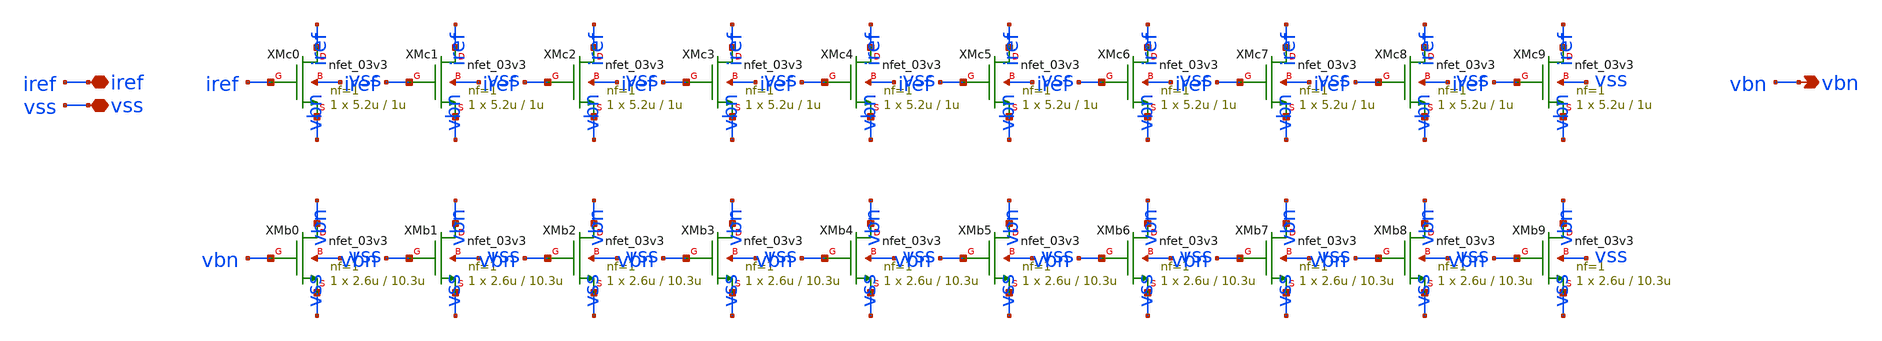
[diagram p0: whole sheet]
** sch_path: design/analog/bias.sch
**.subckt bias iref vss vbn
*.iopin iref
*.iopin vss
*.opin vbn
XMc0 iref iref vbn vss nfet_03v3 L=1u W=5.2u nf=1 ad='int((nf+1)/2) * W/nf * 0.18u' as='int((nf+2)/2) * W/nf * 0.18u'
+ pd='2*int((nf+1)/2) * (W/nf + 0.18u)' ps='2*int((nf+2)/2) * (W/nf + 0.18u)' nrd='0.18u / W' nrs='0.18u / W'
+ sa=0 sb=0 sd=0 m=1
XMb0 vbn vbn vss vss nfet_03v3 L=10.3u W=2.6u nf=1 ad='int((nf+1)/2) * W/nf * 0.18u' as='int((nf+2)/2) * W/nf * 0.18u'
+ pd='2*int((nf+1)/2) * (W/nf + 0.18u)' ps='2*int((nf+2)/2) * (W/nf + 0.18u)' nrd='0.18u / W' nrs='0.18u / W'
+ sa=0 sb=0 sd=0 m=1
XMc1 iref iref vbn vss nfet_03v3 L=1u W=5.2u nf=1 ad='int((nf+1)/2) * W/nf * 0.18u' as='int((nf+2)/2) * W/nf * 0.18u'
+ pd='2*int((nf+1)/2) * (W/nf + 0.18u)' ps='2*int((nf+2)/2) * (W/nf + 0.18u)' nrd='0.18u / W' nrs='0.18u / W'
+ sa=0 sb=0 sd=0 m=1
XMb1 vbn vbn vss vss nfet_03v3 L=10.3u W=2.6u nf=1 ad='int((nf+1)/2) * W/nf * 0.18u' as='int((nf+2)/2) * W/nf * 0.18u'
+ pd='2*int((nf+1)/2) * (W/nf + 0.18u)' ps='2*int((nf+2)/2) * (W/nf + 0.18u)' nrd='0.18u / W' nrs='0.18u / W'
+ sa=0 sb=0 sd=0 m=1
XMc2 iref iref vbn vss nfet_03v3 L=1u W=5.2u nf=1 ad='int((nf+1)/2) * W/nf * 0.18u' as='int((nf+2)/2) * W/nf * 0.18u'
+ pd='2*int((nf+1)/2) * (W/nf + 0.18u)' ps='2*int((nf+2)/2) * (W/nf + 0.18u)' nrd='0.18u / W' nrs='0.18u / W'
+ sa=0 sb=0 sd=0 m=1
XMb2 vbn vbn vss vss nfet_03v3 L=10.3u W=2.6u nf=1 ad='int((nf+1)/2) * W/nf * 0.18u' as='int((nf+2)/2) * W/nf * 0.18u'
+ pd='2*int((nf+1)/2) * (W/nf + 0.18u)' ps='2*int((nf+2)/2) * (W/nf + 0.18u)' nrd='0.18u / W' nrs='0.18u / W'
+ sa=0 sb=0 sd=0 m=1
XMc3 iref iref vbn vss nfet_03v3 L=1u W=5.2u nf=1 ad='int((nf+1)/2) * W/nf * 0.18u' as='int((nf+2)/2) * W/nf * 0.18u'
+ pd='2*int((nf+1)/2) * (W/nf + 0.18u)' ps='2*int((nf+2)/2) * (W/nf + 0.18u)' nrd='0.18u / W' nrs='0.18u / W'
+ sa=0 sb=0 sd=0 m=1
XMb3 vbn vbn vss vss nfet_03v3 L=10.3u W=2.6u nf=1 ad='int((nf+1)/2) * W/nf * 0.18u' as='int((nf+2)/2) * W/nf * 0.18u'
+ pd='2*int((nf+1)/2) * (W/nf + 0.18u)' ps='2*int((nf+2)/2) * (W/nf + 0.18u)' nrd='0.18u / W' nrs='0.18u / W'
+ sa=0 sb=0 sd=0 m=1
XMc4 iref iref vbn vss nfet_03v3 L=1u W=5.2u nf=1 ad='int((nf+1)/2) * W/nf * 0.18u' as='int((nf+2)/2) * W/nf * 0.18u'
+ pd='2*int((nf+1)/2) * (W/nf + 0.18u)' ps='2*int((nf+2)/2) * (W/nf + 0.18u)' nrd='0.18u / W' nrs='0.18u / W'
+ sa=0 sb=0 sd=0 m=1
XMb4 vbn vbn vss vss nfet_03v3 L=10.3u W=2.6u nf=1 ad='int((nf+1)/2) * W/nf * 0.18u' as='int((nf+2)/2) * W/nf * 0.18u'
+ pd='2*int((nf+1)/2) * (W/nf + 0.18u)' ps='2*int((nf+2)/2) * (W/nf + 0.18u)' nrd='0.18u / W' nrs='0.18u / W'
+ sa=0 sb=0 sd=0 m=1
XMc5 iref iref vbn vss nfet_03v3 L=1u W=5.2u nf=1 ad='int((nf+1)/2) * W/nf * 0.18u' as='int((nf+2)/2) * W/nf * 0.18u'
+ pd='2*int((nf+1)/2) * (W/nf + 0.18u)' ps='2*int((nf+2)/2) * (W/nf + 0.18u)' nrd='0.18u / W' nrs='0.18u / W'
+ sa=0 sb=0 sd=0 m=1
XMb5 vbn vbn vss vss nfet_03v3 L=10.3u W=2.6u nf=1 ad='int((nf+1)/2) * W/nf * 0.18u' as='int((nf+2)/2) * W/nf * 0.18u'
+ pd='2*int((nf+1)/2) * (W/nf + 0.18u)' ps='2*int((nf+2)/2) * (W/nf + 0.18u)' nrd='0.18u / W' nrs='0.18u / W'
+ sa=0 sb=0 sd=0 m=1
XMc6 iref iref vbn vss nfet_03v3 L=1u W=5.2u nf=1 ad='int((nf+1)/2) * W/nf * 0.18u' as='int((nf+2)/2) * W/nf * 0.18u'
+ pd='2*int((nf+1)/2) * (W/nf + 0.18u)' ps='2*int((nf+2)/2) * (W/nf + 0.18u)' nrd='0.18u / W' nrs='0.18u / W'
+ sa=0 sb=0 sd=0 m=1
XMb6 vbn vbn vss vss nfet_03v3 L=10.3u W=2.6u nf=1 ad='int((nf+1)/2) * W/nf * 0.18u' as='int((nf+2)/2) * W/nf * 0.18u'
+ pd='2*int((nf+1)/2) * (W/nf + 0.18u)' ps='2*int((nf+2)/2) * (W/nf + 0.18u)' nrd='0.18u / W' nrs='0.18u / W'
+ sa=0 sb=0 sd=0 m=1
XMc7 iref iref vbn vss nfet_03v3 L=1u W=5.2u nf=1 ad='int((nf+1)/2) * W/nf * 0.18u' as='int((nf+2)/2) * W/nf * 0.18u'
+ pd='2*int((nf+1)/2) * (W/nf + 0.18u)' ps='2*int((nf+2)/2) * (W/nf + 0.18u)' nrd='0.18u / W' nrs='0.18u / W'
+ sa=0 sb=0 sd=0 m=1
XMb7 vbn vbn vss vss nfet_03v3 L=10.3u W=2.6u nf=1 ad='int((nf+1)/2) * W/nf * 0.18u' as='int((nf+2)/2) * W/nf * 0.18u'
+ pd='2*int((nf+1)/2) * (W/nf + 0.18u)' ps='2*int((nf+2)/2) * (W/nf + 0.18u)' nrd='0.18u / W' nrs='0.18u / W'
+ sa=0 sb=0 sd=0 m=1
XMc8 iref iref vbn vss nfet_03v3 L=1u W=5.2u nf=1 ad='int((nf+1)/2) * W/nf * 0.18u' as='int((nf+2)/2) * W/nf * 0.18u'
+ pd='2*int((nf+1)/2) * (W/nf + 0.18u)' ps='2*int((nf+2)/2) * (W/nf + 0.18u)' nrd='0.18u / W' nrs='0.18u / W'
+ sa=0 sb=0 sd=0 m=1
XMb8 vbn vbn vss vss nfet_03v3 L=10.3u W=2.6u nf=1 ad='int((nf+1)/2) * W/nf * 0.18u' as='int((nf+2)/2) * W/nf * 0.18u'
+ pd='2*int((nf+1)/2) * (W/nf + 0.18u)' ps='2*int((nf+2)/2) * (W/nf + 0.18u)' nrd='0.18u / W' nrs='0.18u / W'
+ sa=0 sb=0 sd=0 m=1
XMc9 iref iref vbn vss nfet_03v3 L=1u W=5.2u nf=1 ad='int((nf+1)/2) * W/nf * 0.18u' as='int((nf+2)/2) * W/nf * 0.18u'
+ pd='2*int((nf+1)/2) * (W/nf + 0.18u)' ps='2*int((nf+2)/2) * (W/nf + 0.18u)' nrd='0.18u / W' nrs='0.18u / W'
+ sa=0 sb=0 sd=0 m=1
XMb9 vbn vbn vss vss nfet_03v3 L=10.3u W=2.6u nf=1 ad='int((nf+1)/2) * W/nf * 0.18u' as='int((nf+2)/2) * W/nf * 0.18u'
+ pd='2*int((nf+1)/2) * (W/nf + 0.18u)' ps='2*int((nf+2)/2) * (W/nf + 0.18u)' nrd='0.18u / W' nrs='0.18u / W'
+ sa=0 sb=0 sd=0 m=1
**.ends
.end
